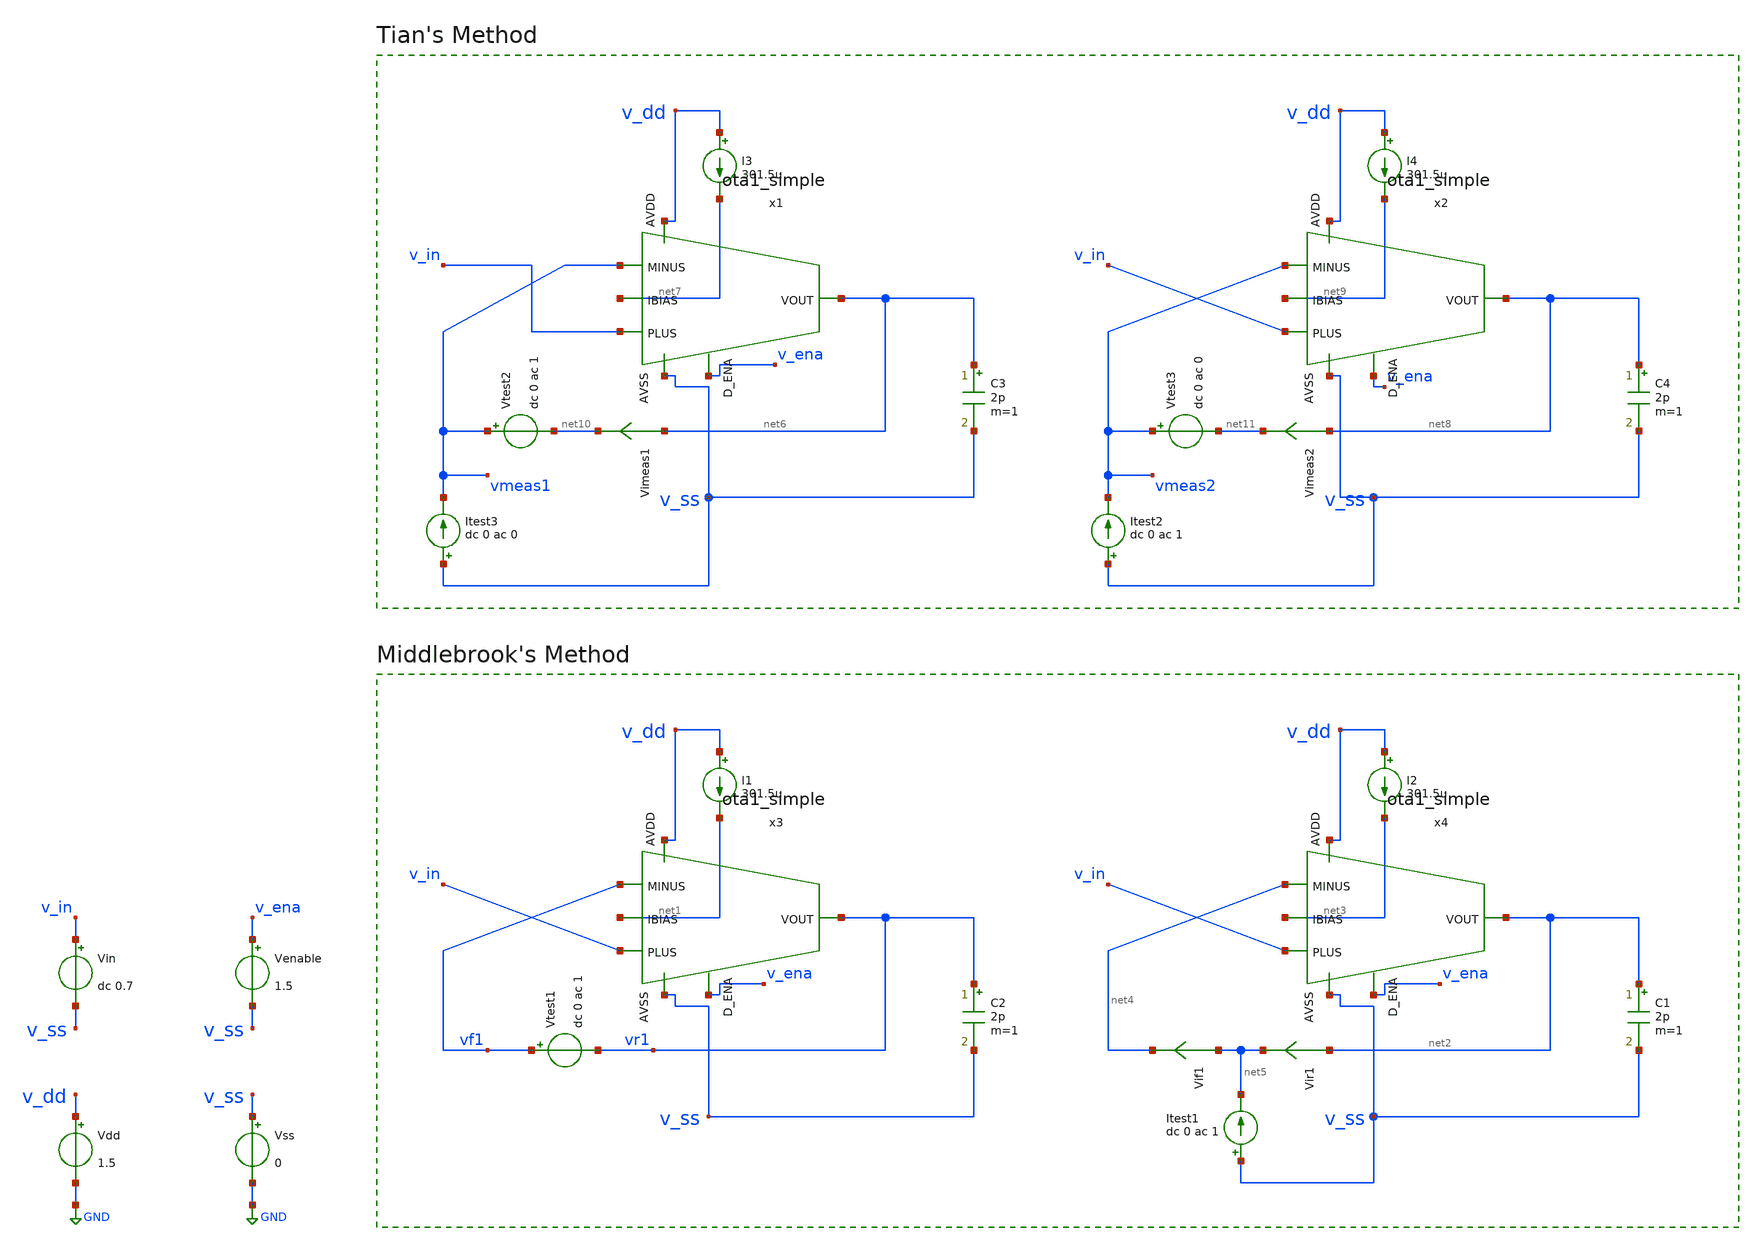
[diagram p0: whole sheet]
** sch_path: DSM_2ndOrder/1_Schematics/real_circuits/loopgain_otasimple.sch
* (c) 2024 H. Pretl, S. Dorrer, Apache-2.0 license
**.subckt loopgain_otasimple
Vdd v_dd GND 1.5
Vss v_ss GND 0
Vin v_in v_ss dc 0.7
Venable v_ena v_ss 1.5
C2 vr1 v_ss 2p m=1
I1 v_dd net1 301.5u
Vtest1 vf1 vr1 dc 0 ac 1
C1 net2 v_ss 2p m=1
I2 v_dd net3 301.5u
Vir1 net2 net5 0
.save i(vir1)
Vif1 net5 net4 0
.save i(vif1)
Itest1 v_ss net5 dc 0 ac 1
C3 net6 v_ss 2p m=1
I3 v_dd net7 301.5u
C4 net8 v_ss 2p m=1
I4 v_dd net9 301.5u
Itest3 v_ss vmeas1 dc 0 ac 0
Vtest2 vmeas1 net10 dc 0 ac 1
Vimeas1 net6 net10 0
.save i(vimeas1)
Itest2 v_ss vmeas2 dc 0 ac 1
Vtest3 vmeas2 net11 dc 0 ac 0
Vimeas2 net8 net11 0
.save i(vimeas2)
x1 v_dd v_in vmeas1 net6 net7 v_ena v_ss ota1_simple
x2 v_dd v_in vmeas2 net8 net9 v_ena v_ss ota1_simple
x3 v_dd v_in vf1 vr1 net1 v_ena v_ss ota1_simple
x4 v_dd v_in net4 net2 net3 v_ena v_ss ota1_simple
**** begin user architecture code

.lib cornerMOSlv.lib mos_tt
.lib cornerRES.lib res_typ



.param temp=27
.options savecurrents reltol=1e-3 abstol=1e-12 gmin=1e-15
.control
save all

* Operating Point Analysis
op
remzerovec
write ota-improved_tb-loopgain.raw
set appendwrite

* AC Analysis
ac dec 101 1 100G
remzerovec
write ota-improved_tb-loopgain.raw
set appendwrite

* Middlebrook's Method
let tv=-v(vr1)/v(vf1)
let ti=-i(vir1)/i(vif1)
let tmb=(tv*ti - 1)/(tv + ti + 2)

plot db(tmb) ylabel 'Magnitude - Middlebrook'
plot 180/pi*cphase(tmb) ylabel 'Phase - Middlebrook'

* Tian's Method
* vtest=0, itest=1:
let A=i(Vimeas2)
let C=v(vmeas2)

* vtest=1, itest=0:
let B=i(Vimeas1)
let D=v(vmeas1)
let ttian=(A*D-B*C-A)/(2*(B*C-A*D)+A-D+1)

plot db(ttian) ylabel 'Magnitude - Tian'
plot 180/pi*cphase(ttian) ylabel 'Phase - Tian'

* Middlebrook vs. Tian
plot db(tmb) db(ttian) ylabel 'Magnitude'
plot 180/pi*cphase(tmb) 180/pi*cphase(ttian) ylabel 'Phase'

write ota-improved_tb-loopgain.raw

*quit
.endc


**** end user architecture code
**.ends

* expanding   symbol:  ota1_simple.sym # of pins=7
** sym_path: DSM_2ndOrder/1_Schematics/real_circuits/3v3/ota1_simple.sym
** sch_path: DSM_2ndOrder/1_Schematics/real_circuits/3v3/ota1_simple.sch
.subckt ota1_simple AVDD PLUS MINUS VOUT IBIAS D_ENA AVSS
*.opin VOUT
*.ipin MINUS
*.ipin PLUS
*.ipin AVSS
*.ipin IBIAS
*.ipin AVDD
*.ipin D_ENA
XM01 net9 PLUS net1 AVSS sg13_lv_nmos w=161.5u l=2u ng=17 m=1 mm_ok=1
XM02 net10 MINUS net1 AVSS sg13_lv_nmos w=161.5u l=2u ng=17 m=1 mm_ok=1
XMt net1 net6 AVSS AVSS sg13_lv_nmos w=38u l=1u ng=4 m=1 mm_ok=1
XM08 VOUT net2 net5 AVSS sg13_lv_nmos w=95u l=1.5u ng=10 m=1 mm_ok=1
XM07 net3 net2 net4 AVSS sg13_lv_nmos w=95u l=1.5u ng=10 m=1 mm_ok=1
XM03 net4 net3 AVSS AVSS sg13_lv_nmos w=95u l=1.5u ng=10 m=1 mm_ok=1
XM04 net5 net3 AVSS AVSS sg13_lv_nmos w=95u l=1.5u ng=10 m=1 mm_ok=1
XMb1 net11 net6 AVSS AVSS sg13_lv_nmos w=38u l=1u ng=4 m=1 mm_ok=1
XM05 net3 net7 net9 AVDD sg13_lv_pmos w=385u l=1.5u ng=39 m=1 mm_ok=1
XM06 VOUT net7 net10 AVDD sg13_lv_pmos w=385u l=1.5u ng=39 m=1 mm_ok=1
XM09 net9 net8 AVDD AVDD sg13_lv_pmos w=500u l=1.5u ng=50 m=1 mm_ok=1
XM10 net10 net8 AVDD AVDD sg13_lv_pmos w=500u l=1.5u ng=50 m=1 mm_ok=1
XMb IBIAS net6 AVSS AVSS sg13_lv_nmos w=38u l=1u ng=4 m=1 mm_ok=1
XMb2 net11 net3 net8 AVDD sg13_lv_pmos w=385u l=1.5u ng=39 m=1 mm_ok=1
XMb3 net8 net8 AVDD AVDD sg13_lv_pmos w=385u l=1.5u ng=39 m=1 mm_ok=1
XMb5 net7 net8 AVDD AVDD sg13_lv_pmos w=385u l=1.5u ng=39 m=1 mm_ok=1
XMb4 AVSS net3 net7 AVDD sg13_lv_pmos w=50u l=0.5u ng=5 m=1 mm_ok=1
XMb10 AVDD VOUT net2 AVSS sg13_lv_nmos w=0.15u l=0.13u ng=1 m=1 mm_ok=1
XMb9 net2 net12 AVSS AVSS sg13_lv_nmos w=0.15u l=0.13u ng=1 m=1 mm_ok=1
XMb7 net8 VOUT net12 AVSS sg13_lv_nmos w=95u l=1.5u ng=10 m=1 mm_ok=1
XMb8 net12 net12 AVSS AVSS sg13_lv_nmos w=95u l=1.5u ng=10 m=1 mm_ok=1
XMb6 net8 net8 AVDD AVDD sg13_lv_pmos w=500u l=1.5u ng=50 m=1 mm_ok=1
XMe5 IBIAS net14 net6 AVSS sg13_lv_nmos w=1u l=0.13u ng=1 m=1 mm_ok=1
XMe2 net13 D_ENA AVSS AVSS sg13_lv_nmos w=1u l=0.13u ng=1 m=1 mm_ok=1
XMe4 net14 net13 AVSS AVSS sg13_lv_nmos w=1u l=0.13u ng=1 m=1 mm_ok=1
XMe6 net3 net13 AVSS AVSS sg13_lv_nmos w=1u l=0.13u ng=1 m=1 mm_ok=1
XMe3 net14 net13 AVDD AVDD sg13_lv_pmos w=1u l=0.13u ng=1 m=1 mm_ok=1
XMe1 net13 D_ENA AVDD AVDD sg13_lv_pmos w=1u l=0.13u ng=1 m=1 mm_ok=1
.ends

.GLOBAL GND
.end
